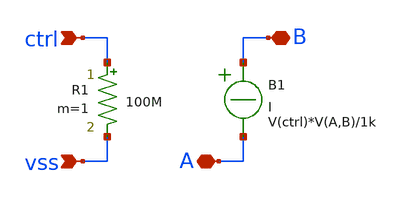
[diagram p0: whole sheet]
** sch_path: design/JNW_AVV_SKY130A/ideal_switch.sch
**.subckt ideal_switch ctrl A B vss
*.ipin ctrl
*.iopin A
*.iopin B
*.ipin vss
B1 B A I = V(ctrl)*V(A,B)/1k

R1 ctrl vss 100M m=1
**.ends
.end
